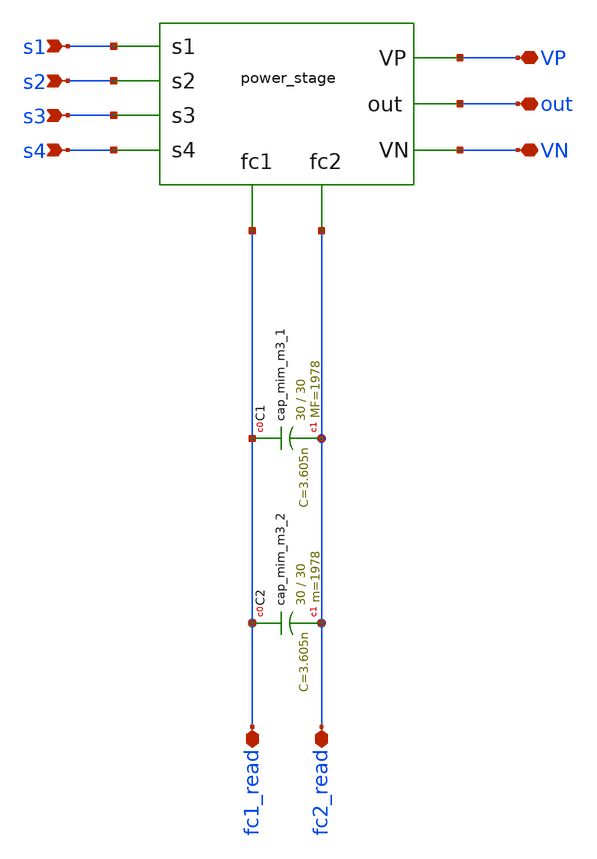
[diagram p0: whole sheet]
** sch_path: ISSCC23/submitted_notebooks/3LFCC/symbols/converter.sch
**.subckt converter s1 s2 s3 s4 VP VN out fc2_read fc1_read
*.ipin s1
*.ipin s2
*.ipin s3
*.ipin s4
*.iopin VP
*.iopin VN
*.iopin out
*.iopin fc2_read
*.iopin fc1_read
X1v s1 s2 s3 s4 fc1_read fc2_read out VP VN power_stage
XC1 fc1_read fc2_read sky130_fd_pr__cap_mim_m3_1 W=30 L=30 MF=1978 m=1978
XC2 fc1_read fc2_read sky130_fd_pr__cap_mim_m3_2 W=30 L=30 MF=1978 m=1978
**.ends
.end
